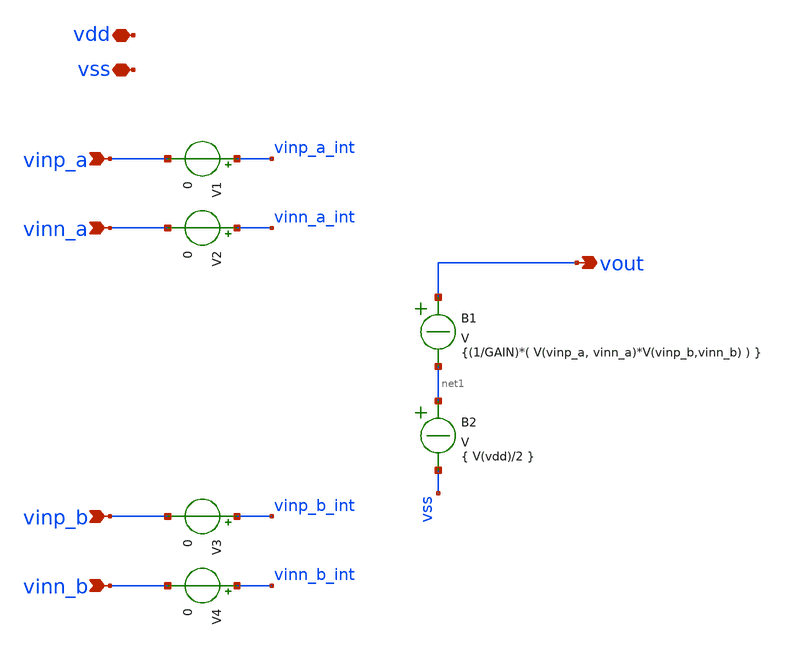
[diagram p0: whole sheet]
** sch_path: xsch/behavioral/multiplier.sch
**.subckt multiplier vinp_a vinn_a vout vss vinp_b vinn_b vdd
*.ipin vinp_a
*.ipin vinn_a
*.opin vout
*.iopin vss
*.ipin vinp_b
*.ipin vinn_b
*.iopin vdd
V1 vinp_a_int vinp_a 0
V2 vinn_a_int vinn_a 0
B1 vout net1 V = {(1/GAIN)*( V(vinp_a, vinn_a)*V(vinp_b,vinn_b) ) }
V3 vinp_b_int vinp_b 0
V4 vinn_b_int vinn_b 0
B2 net1 vss V = { V(vdd)/2 }
**.ends
.end
